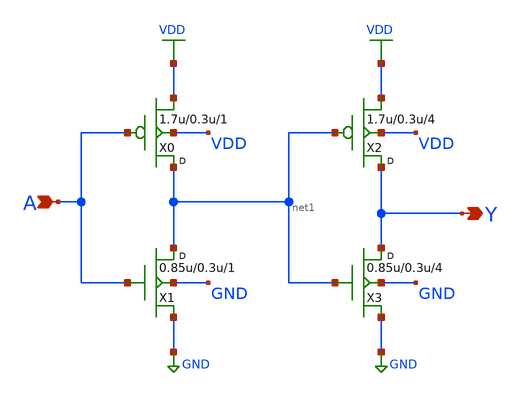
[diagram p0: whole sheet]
** sch_path: gf180mcu_osu_sc_gp9t3v3/cells/buf/gf180mcu_osu_sc_gp9t3v3__buf_4.sch
**.subckt gf180mcu_osu_sc_gp9t3v3__buf_4 A Y
*.ipin A
*.opin Y
X0 net1 A VDD VDD pfet_03p3 w=1.7u l=0.3u m=1
X1 net1 A GND GND nfet_03p3 w=0.85u l=0.3u m=1
X2 Y net1 VDD VDD pfet_03p3 w=1.7u l=0.3u m=4
X3 Y net1 GND GND nfet_03p3 w=0.85u l=0.3u m=4
**.ends
.GLOBAL VDD
.GLOBAL GND
.end
